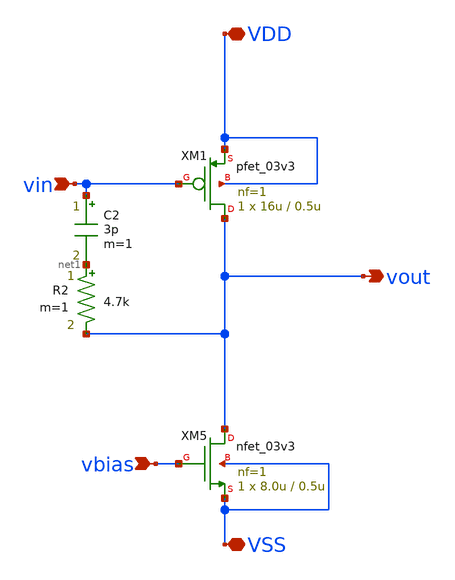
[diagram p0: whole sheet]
** sch_path: xschem/amp_stg_2.sch
**.subckt amp_stg_2 vin vbias VSS VDD vout
*.ipin vin
*.ipin vbias
*.iopin VSS
*.iopin VDD
*.opin vout
XM1 vout vin VDD VDD pfet_03v3 L=0.5u W=16u nf=1 ad='int((nf+1)/2) * W/nf * 0.18u' as='int((nf+2)/2) * W/nf * 0.18u'
+ pd='2*int((nf+1)/2) * (W/nf + 0.18u)' ps='2*int((nf+2)/2) * (W/nf + 0.18u)' nrd='0.18u / W' nrs='0.18u / W'
+ sa=0 sb=0 sd=0 m=1 par=1
XM5 vout vbias VSS VSS nfet_03v3 L=0.5u W=8.0u nf=1 ad='int((nf+1)/2) * W/nf * 0.18u' as='int((nf+2)/2) * W/nf * 0.18u'
+ pd='2*int((nf+1)/2) * (W/nf + 0.18u)' ps='2*int((nf+2)/2) * (W/nf + 0.18u)' nrd='0.18u / W' nrs='0.18u / W'
+ sa=0 sb=0 sd=0 m=1 par=1
C2 vin net1 3p m=1
R2 net1 vout 4.7k m=1
**.ends
.end
